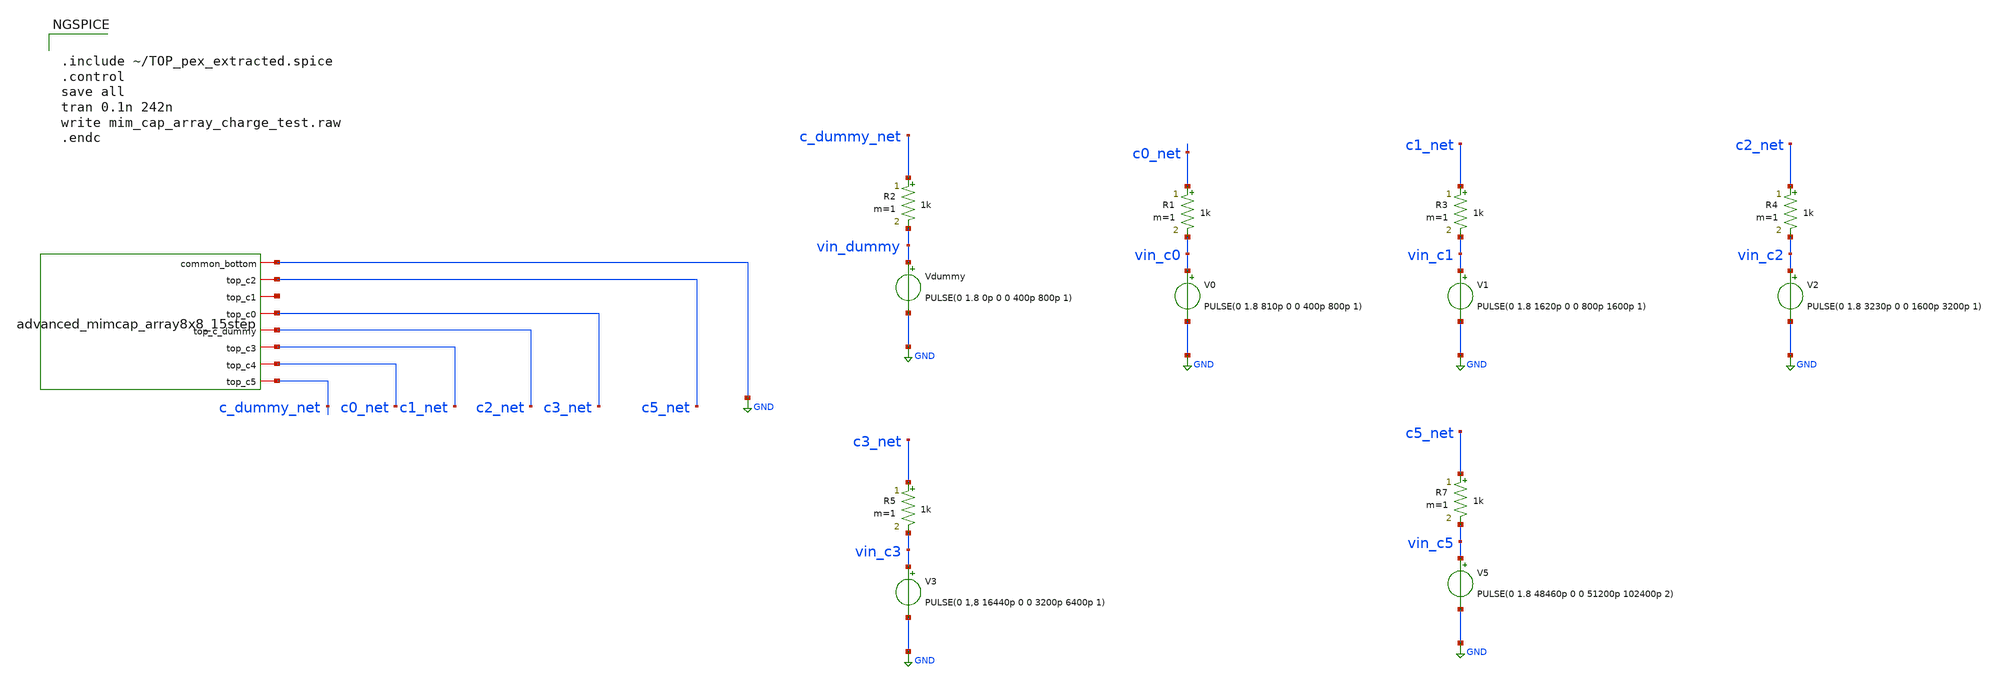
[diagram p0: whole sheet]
** sch_path: cdac/mim_cap_array_8x8/tb/mim_cap_array_charge_test.sch
* Copyright 2022 GlobalFoundries PDK Authors
* Licensed under the Apache License, Version 2.0 (the "License");
* you may not use this file except in compliance with the License.
* You may obtain a copy of the License at
* https://www.apache.org/licenses/LICENSE-2.0
* Unless required by applicable law or agreed to in writing, software
* distributed under the License is distributed on an "AS IS" BASIS,
* WITHOUT WARRANTIES OR CONDITIONS OF ANY KIND, either express or implied.
* See the License for the specific language governing permissions and
* limitations under the License.
**.subckt mim_cap_array_charge_test
Vdummy vin_dummy GND PULSE(0 1.8 0p 0 0 400p 800p 1)
R2 c_dummy_net vin_dummy 1k m=1
V0 vin_c0 GND PULSE(0 1.8 810p 0 0 400p 800p 1)
R1 c0_net vin_c0 1k m=1
V1 vin_c1 GND PULSE(0 1.8 1620p 0 0 800p 1600p 1)
R3 c1_net vin_c1 1k m=1
V2 vin_c2 GND PULSE(0 1.8 3230p 0 0 1600p 3200p 1)
R4 c2_net vin_c2 1k m=1
V3 vin_c3 GND PULSE(0 1,8 16440p 0 0 3200p 6400p 1)
R5 c3_net vin_c3 1k m=1
V5 vin_c5 GND PULSE(0 1.8 48460p 0 0 51200p 102400p 2)
R7 c5_net vin_c5 1k m=1
x1 c_dummy_net c1_net c5_net c0_net c3_net net1 c2_net GND TOP
**** begin user architecture code

.include $::180MCU_MODELS/design.ngspice
.lib $::180MCU_MODELS/sm141064.ngspice typical
.lib $::180MCU_MODELS/sm141064.ngspice cap_mim
.lib $::180MCU_MODELS/sm141064.ngspice res_typical
.lib $::180MCU_MODELS/sm141064.ngspice moscap_typical
.lib $::180MCU_MODELS/sm141064.ngspice mimcap_typical
* .lib $::180MCU_MODELS/sm141064.ngspice res_statistical



.include ~/TOP_pex_extracted.spice
.control
save all
tran 0.1n 242n
write mim_cap_array_charge_test.raw
.endc


**** end user architecture code
**.ends
.GLOBAL GND
.end
